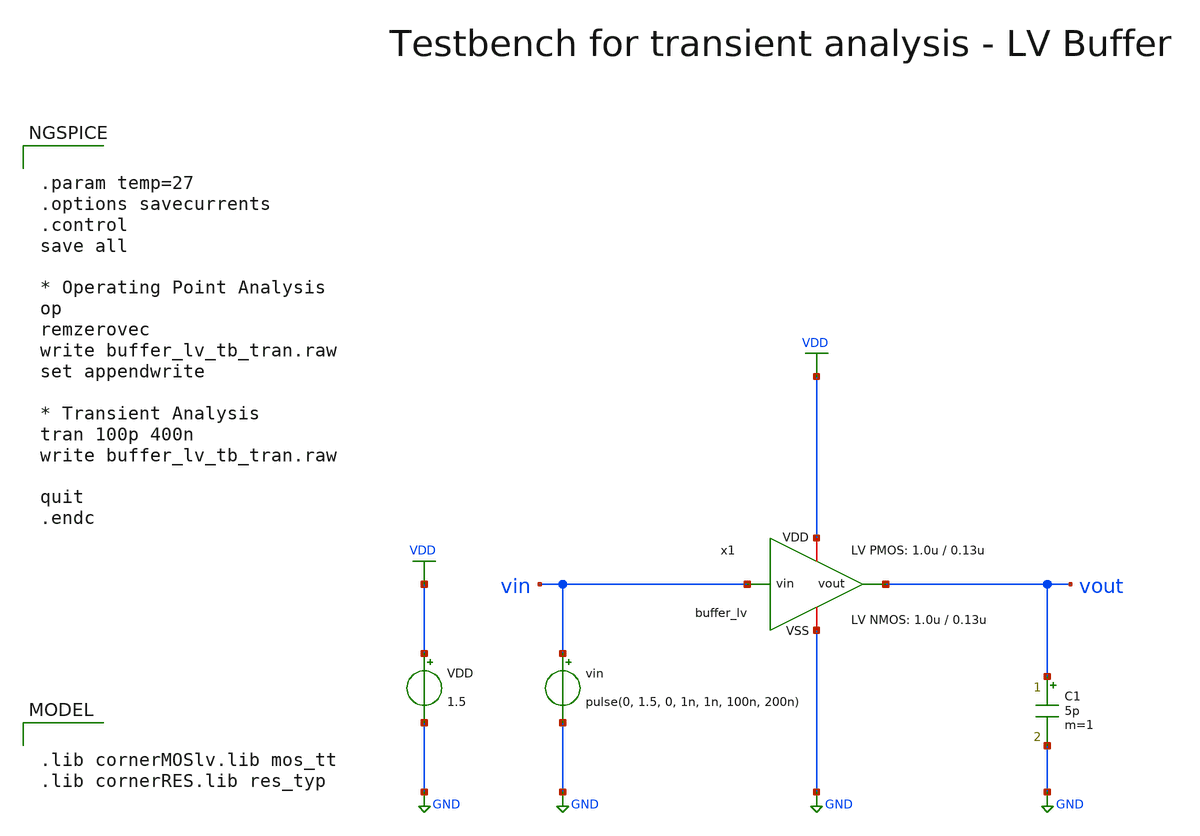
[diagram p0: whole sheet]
** sch_path: SG13G2_ATBS-ADC-main/xschem/buffer/testbenches/buffer_lv_tb_tran.sch
**.subckt buffer_lv_tb_tran
VDD VDD GND 1.5
vin vin GND pulse(0, 1.5, 0, 1n, 1n, 100n, 200n)
C1 vout GND 5p m=1
x1 VDD vin vout GND buffer_lv W_P_INV=1.0u L_P_INV=0.13u W_N_INV=1.0u L_N_INV=0.13u
**** begin user architecture code

.lib cornerMOSlv.lib mos_tt
.lib cornerRES.lib res_typ



.param temp=27
.options savecurrents
.control
save all

* Operating Point Analysis
op
remzerovec
write buffer_lv_tb_tran.raw
set appendwrite

* Transient Analysis
tran 100p 400n
write buffer_lv_tb_tran.raw

quit
.endc


**** end user architecture code
**.ends

* expanding   symbol:  buffer/buffer_lv.sym # of pins=4
** sym_path: SG13G2_ATBS-ADC-main/xschem/buffer/buffer_lv.sym
** sch_path: SG13G2_ATBS-ADC-main/xschem/buffer/buffer_lv.sch
.subckt buffer_lv VDD vin vout VSS  W_P_INV=3.0u L_P_INV=0.13u W_N_INV=1.0u L_N_INV=0.13u
*.ipin vin
*.iopin VDD
*.iopin VSS
*.opin vout
x1 VDD vin net1 VSS inverter_lv W_P=W_P_INV L_P=L_P_INV W_N=W_N_INV L_N=L_N_INV
x2 VDD net1 vout VSS inverter_lv W_P=W_P_INV L_P=L_P_INV W_N=W_N_INV L_N=L_N_INV
.ends


* expanding   symbol:  inverter/inverter_lv.sym # of pins=4
** sym_path: SG13G2_ATBS-ADC-main/xschem/inverter/inverter_lv.sym
** sch_path: SG13G2_ATBS-ADC-main/xschem/inverter/inverter_lv.sch
.subckt inverter_lv VDD vin vout VSS  W_P=3.0u L_P=0.13u W_N=1.0u L_N=0.13u
*.ipin vin
*.iopin VDD
*.iopin VSS
*.opin vout
XM1 vout vin VDD VDD sg13_lv_pmos w=W_P l=L_P ng=1 m=1 mm_ok=1
XM2 vout vin VSS VSS sg13_lv_nmos w=W_N l=L_N ng=1 m=1 mm_ok=1
.ends

.GLOBAL GND
.GLOBAL VDD
.end
